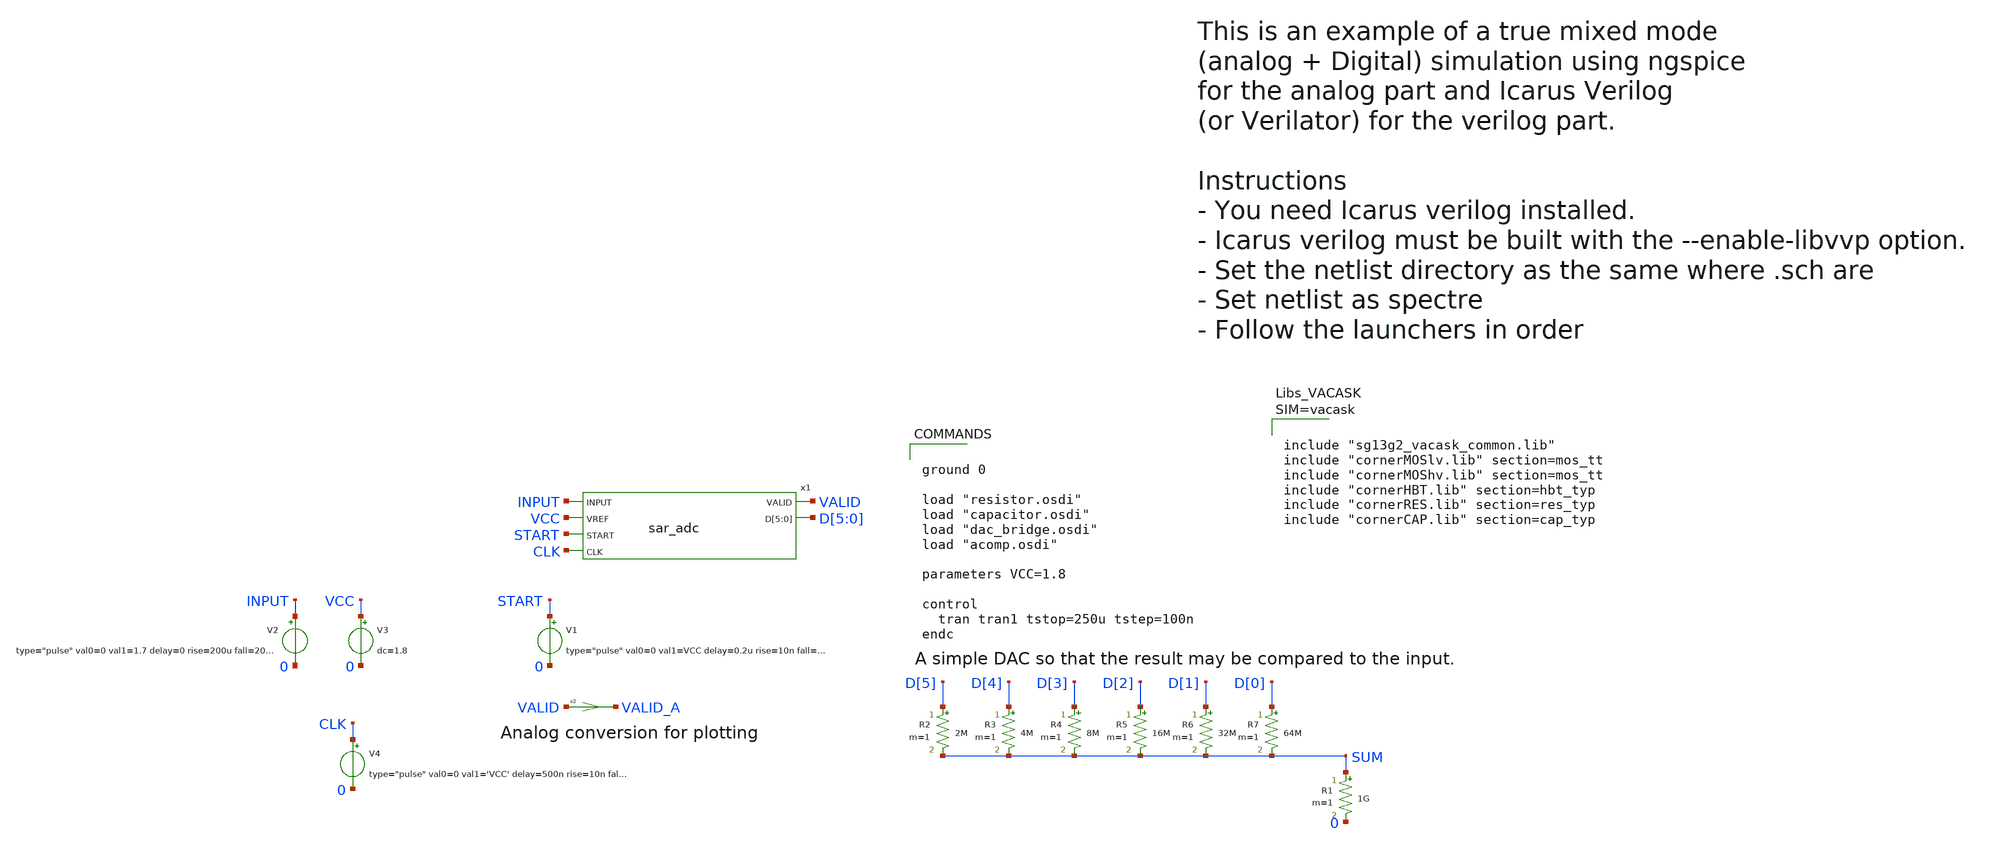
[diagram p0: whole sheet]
** sch_path: demo/cosim/vacask_cosim_hier/tb_sar_adc.sch
**.subckt tb_sar_adc
R2 D[5] SUM 2M m=1
R3 D[4] SUM 4M m=1
R4 D[3] SUM 8M m=1
R5 D[2] SUM 16M m=1
R6 D[1] SUM 32M m=1
R7 D[0] SUM 64M m=1
V3 VCC 0 dc=1.8
V2 INPUT 0 type="pulse" val0=0 val1=1.7 delay=0 rise=200u fall=200u width=1u period=402u
V1 START 0 type="pulse" val0=0 val1=VCC delay=0.2u rise=10n fall=10n width=1.3u period=10u
V4 CLK 0 type="pulse" val0=0 val1='VCC' delay=500n rise=10n fall=10n width=490n period=1u
x1 INPUT VCC START VALID D[5] D[4] D[3] D[2] D[1] D[0] CLK sar_adc
x2 VALID_A VALID dac_bridge
R1 SUM 0 1G m=1
**** begin user architecture code


ground 0

load "resistor.osdi"
load "capacitor.osdi"
load "dac_bridge.osdi"
load "acomp.osdi"

parameters VCC=1.8

control
  tran tran1 tstop=250u tstep=100n
endc





**** end user architecture code
**.ends
.end
